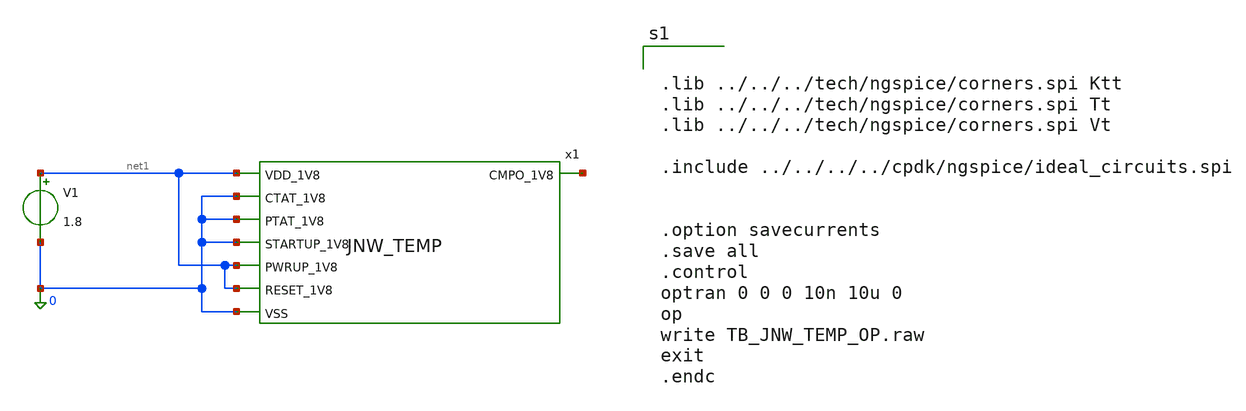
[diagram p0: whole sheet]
** sch_path: design/JNW_TEMP_SKY130A/TB_JNW_TEMP_OP.sch
**.subckt TB_JNW_TEMP_OP
x1 net1 0 0 0 net2 net1 net1 0 JNW_TEMP
V1 net1 0 1.8
**** begin user architecture code


.lib ../../../tech/ngspice/corners.spi Ktt
.lib ../../../tech/ngspice/corners.spi Tt
.lib ../../../tech/ngspice/corners.spi Vt

.include ../../../../cpdk/ngspice/ideal_circuits.spi


.option savecurrents
.save all
.control
optran 0 0 0 10n 10u 0
op
write TB_JNW_TEMP_OP.raw
exit
.endc



**** end user architecture code
**.ends
.end
